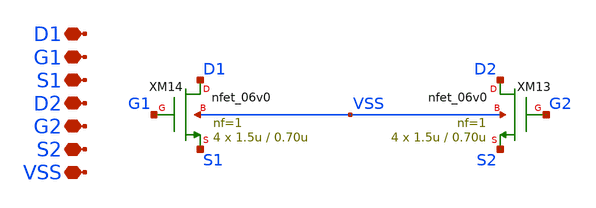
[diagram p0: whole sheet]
** sch_path: designs/libs/core_single-fet/nfet-vss/nfet-vss.sch
**.subckt nfet-vss VSS S2 G2 D2 S1 G1 D1
*.iopin VSS
*.iopin S2
*.iopin G2
*.iopin D2
*.iopin S1
*.iopin G1
*.iopin D1
XM13 D2 G2 S2 VSS nfet_06v0 L=0.70u W=1.5u nf=1 ad='int((nf+1)/2) * W/nf * 0.18u' as='int((nf+2)/2) * W/nf * 0.18u'
+ pd='2*int((nf+1)/2) * (W/nf + 0.18u)' ps='2*int((nf+2)/2) * (W/nf + 0.18u)' nrd='0.18u / W' nrs='0.18u / W'
+ sa=0 sb=0 sd=0 m=4
XM14 D1 G1 S1 VSS nfet_06v0 L=0.70u W=1.5u nf=1 ad='int((nf+1)/2) * W/nf * 0.18u' as='int((nf+2)/2) * W/nf * 0.18u'
+ pd='2*int((nf+1)/2) * (W/nf + 0.18u)' ps='2*int((nf+2)/2) * (W/nf + 0.18u)' nrd='0.18u / W' nrs='0.18u / W'
+ sa=0 sb=0 sd=0 m=4
**.ends
.end
